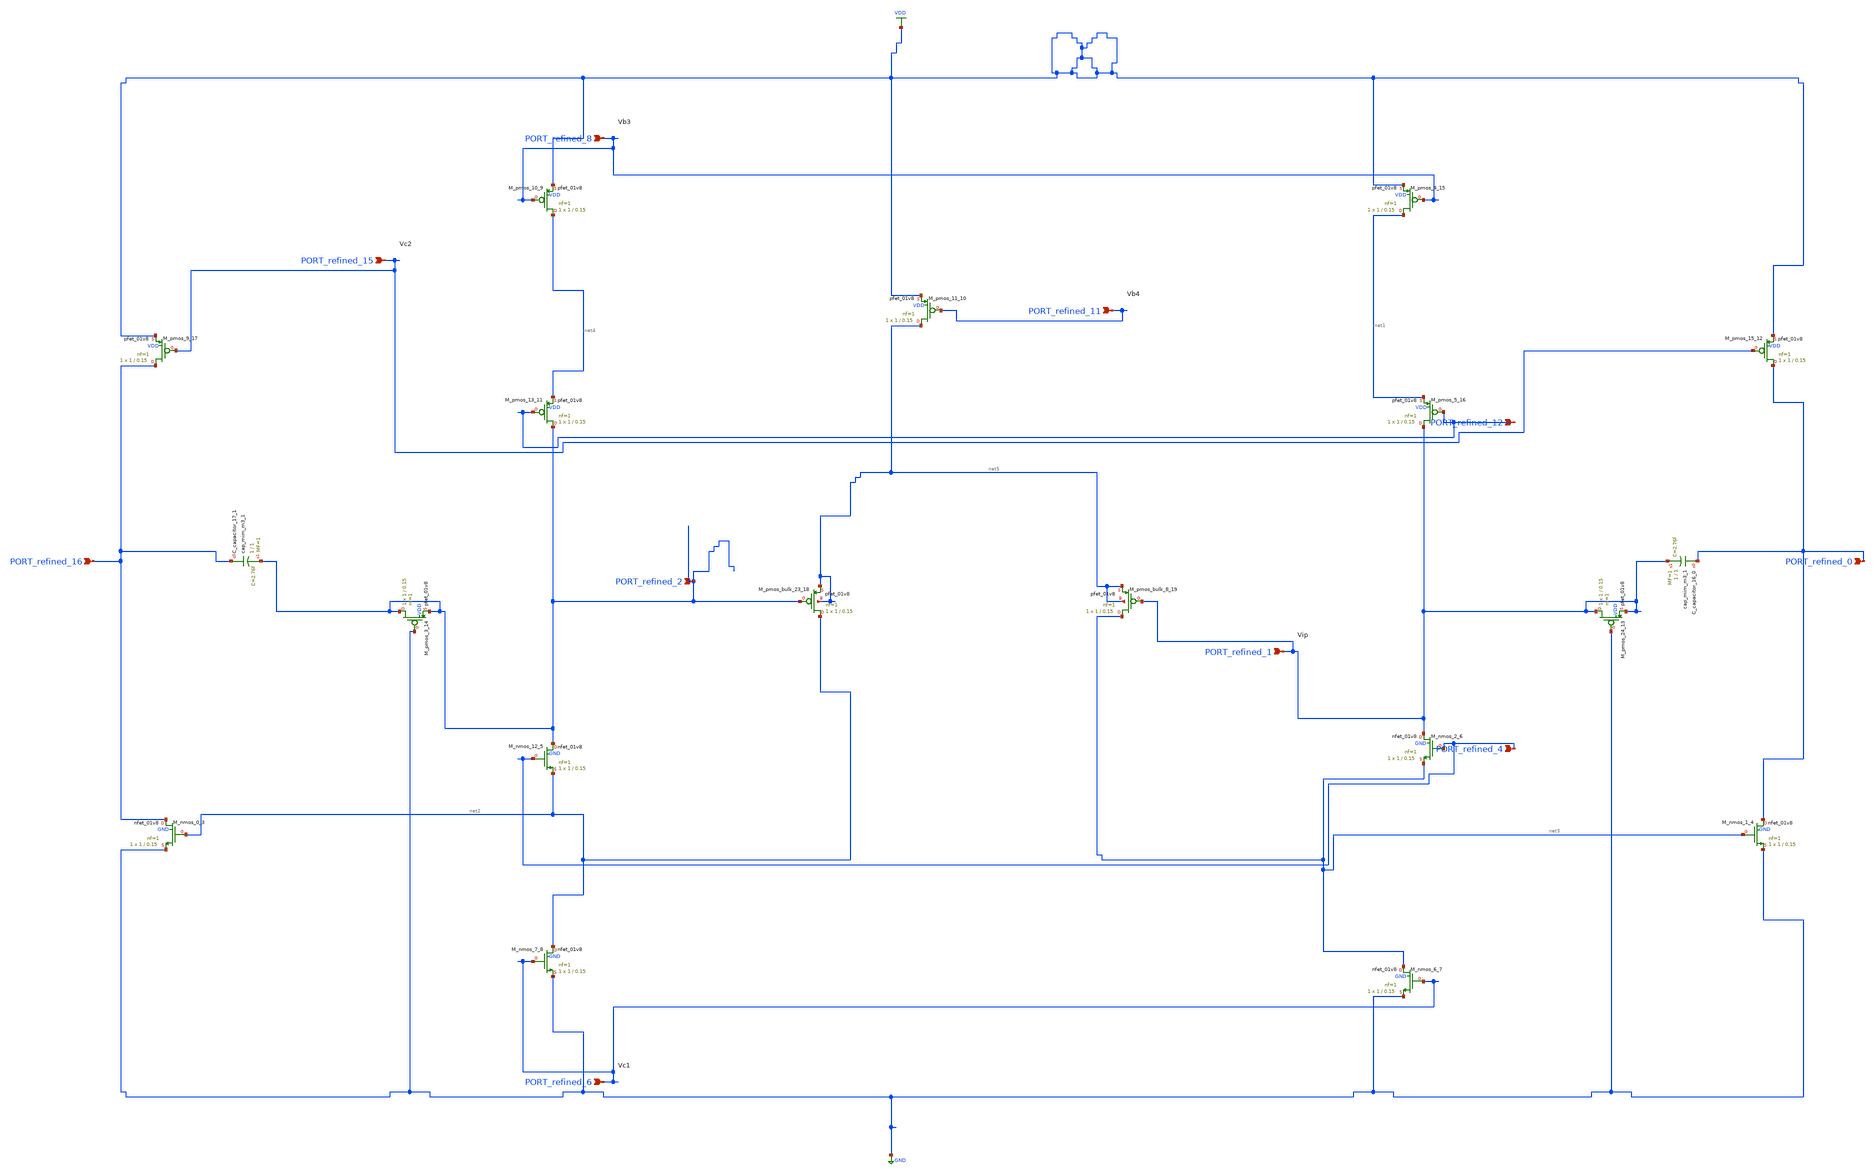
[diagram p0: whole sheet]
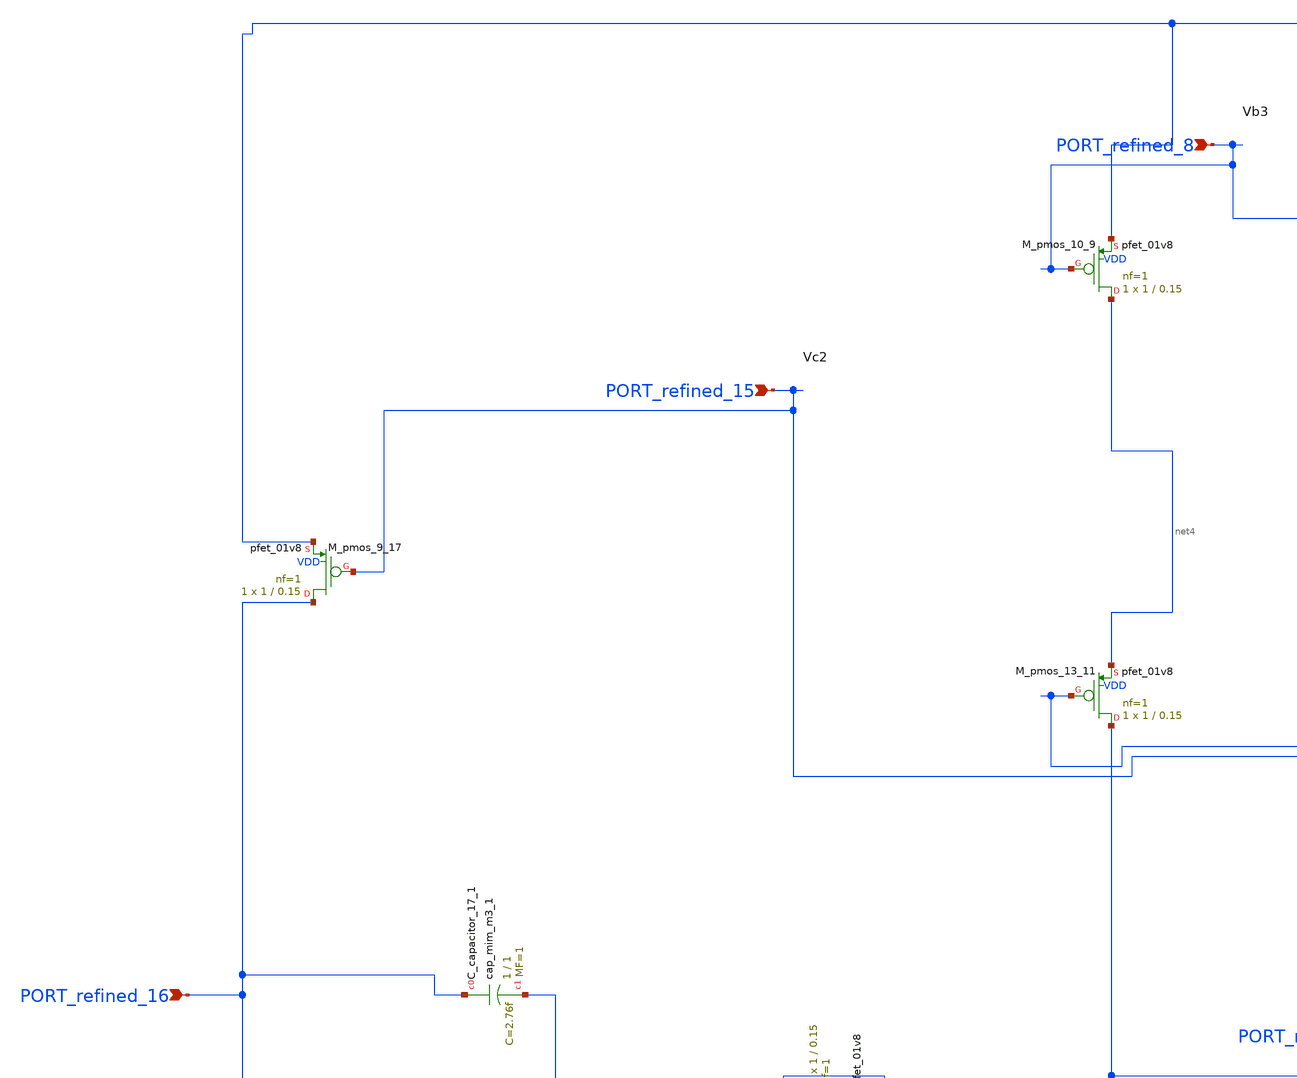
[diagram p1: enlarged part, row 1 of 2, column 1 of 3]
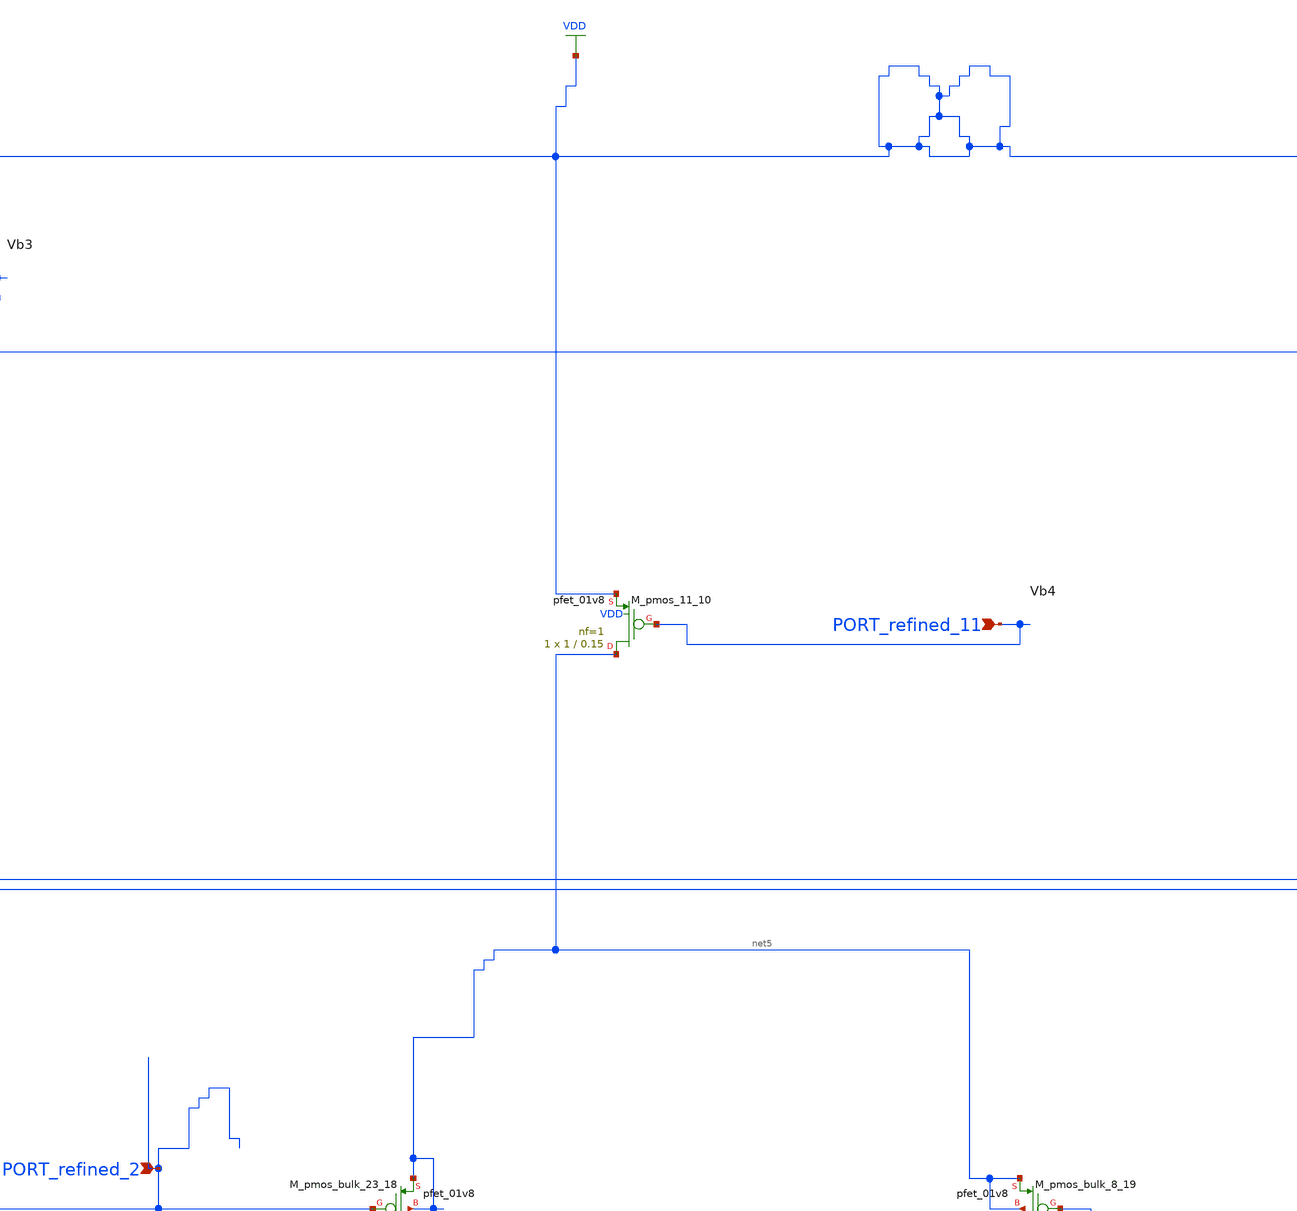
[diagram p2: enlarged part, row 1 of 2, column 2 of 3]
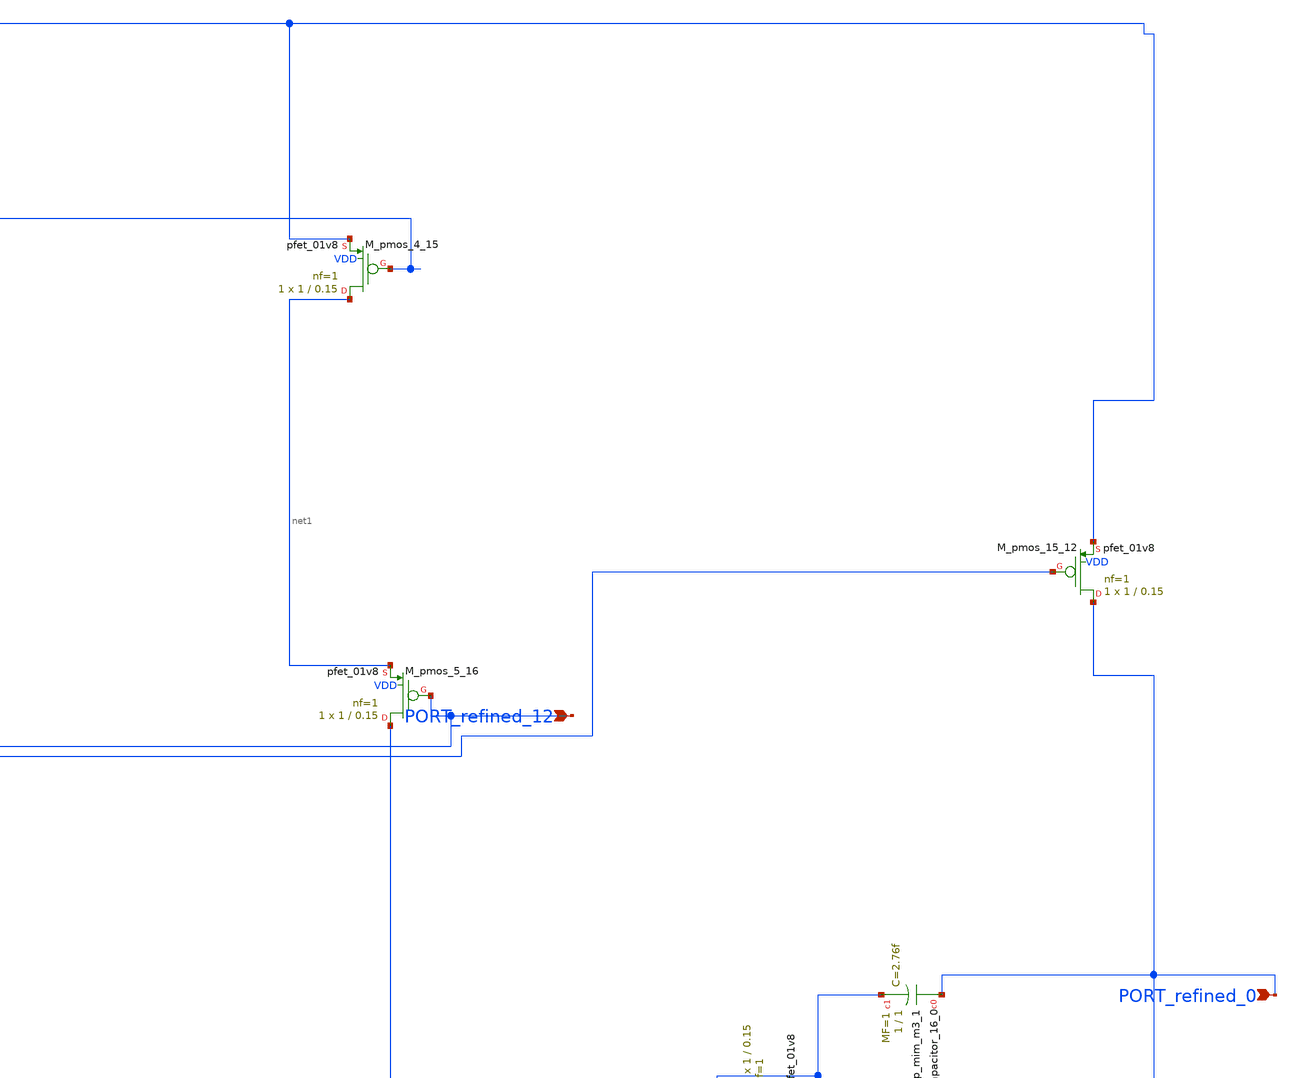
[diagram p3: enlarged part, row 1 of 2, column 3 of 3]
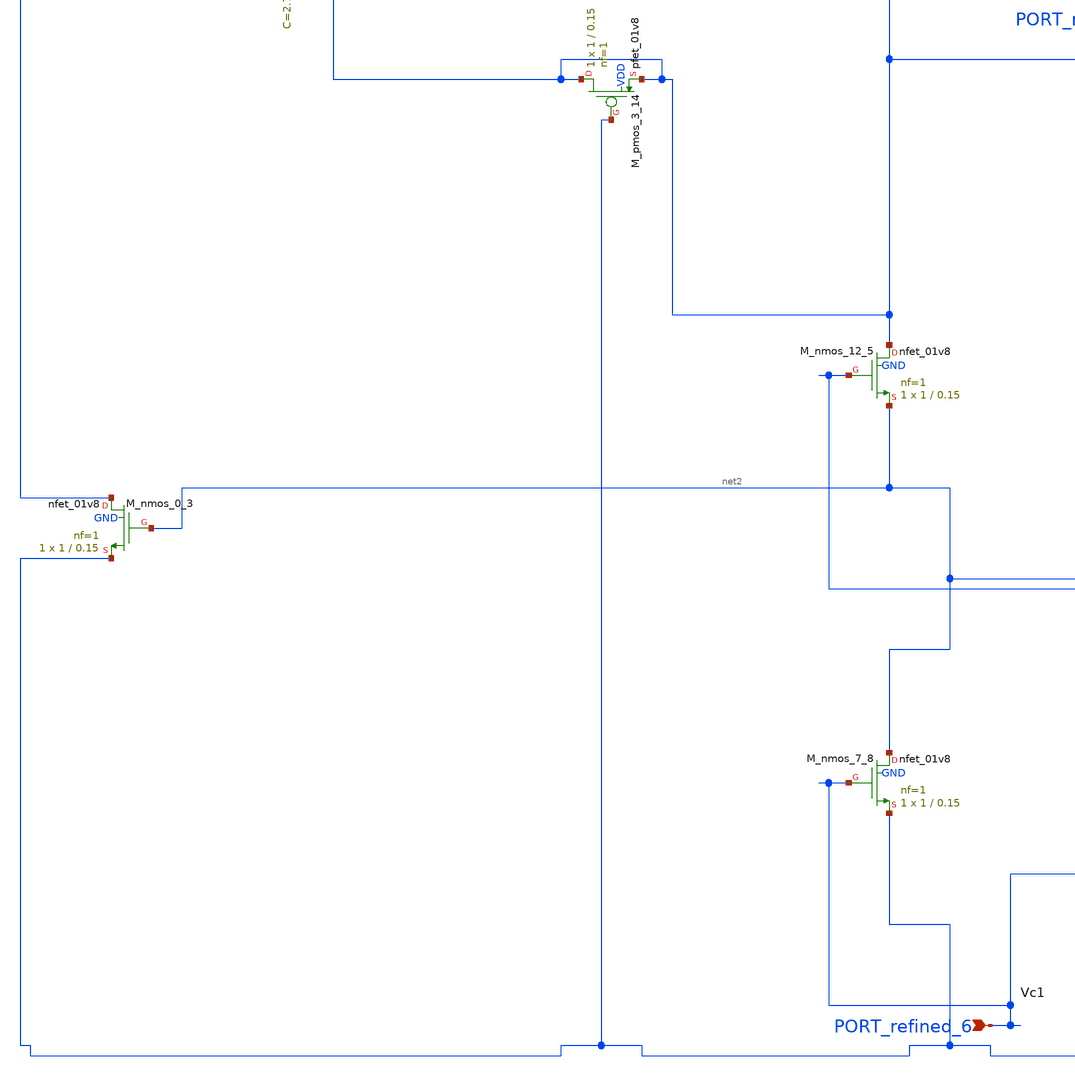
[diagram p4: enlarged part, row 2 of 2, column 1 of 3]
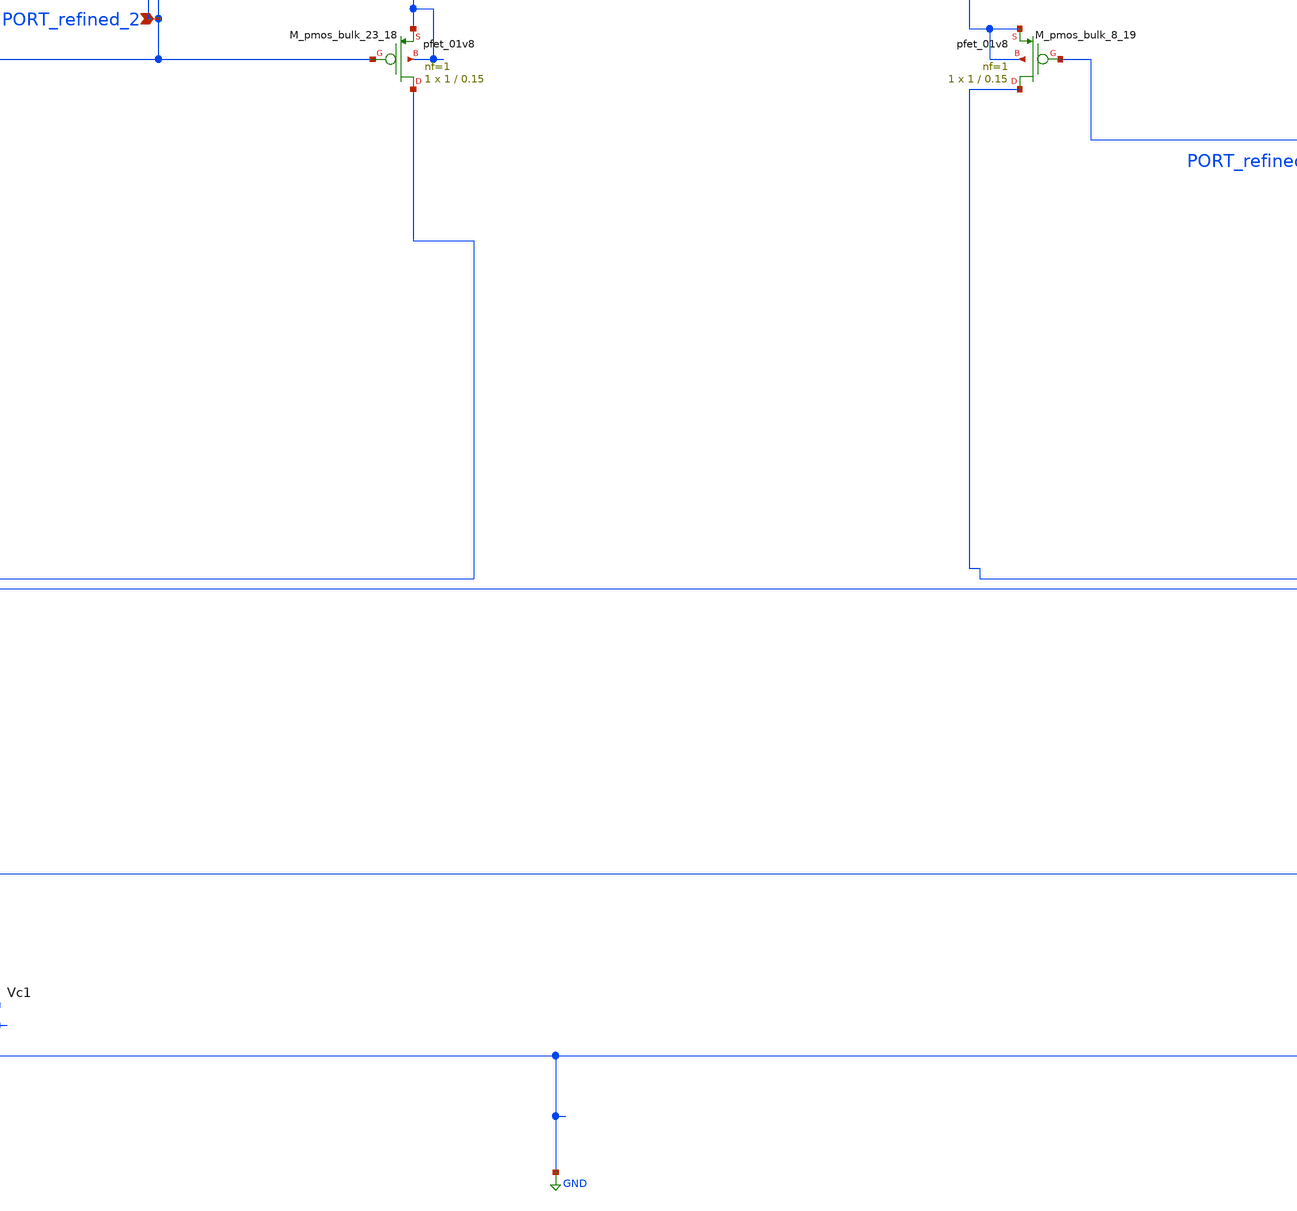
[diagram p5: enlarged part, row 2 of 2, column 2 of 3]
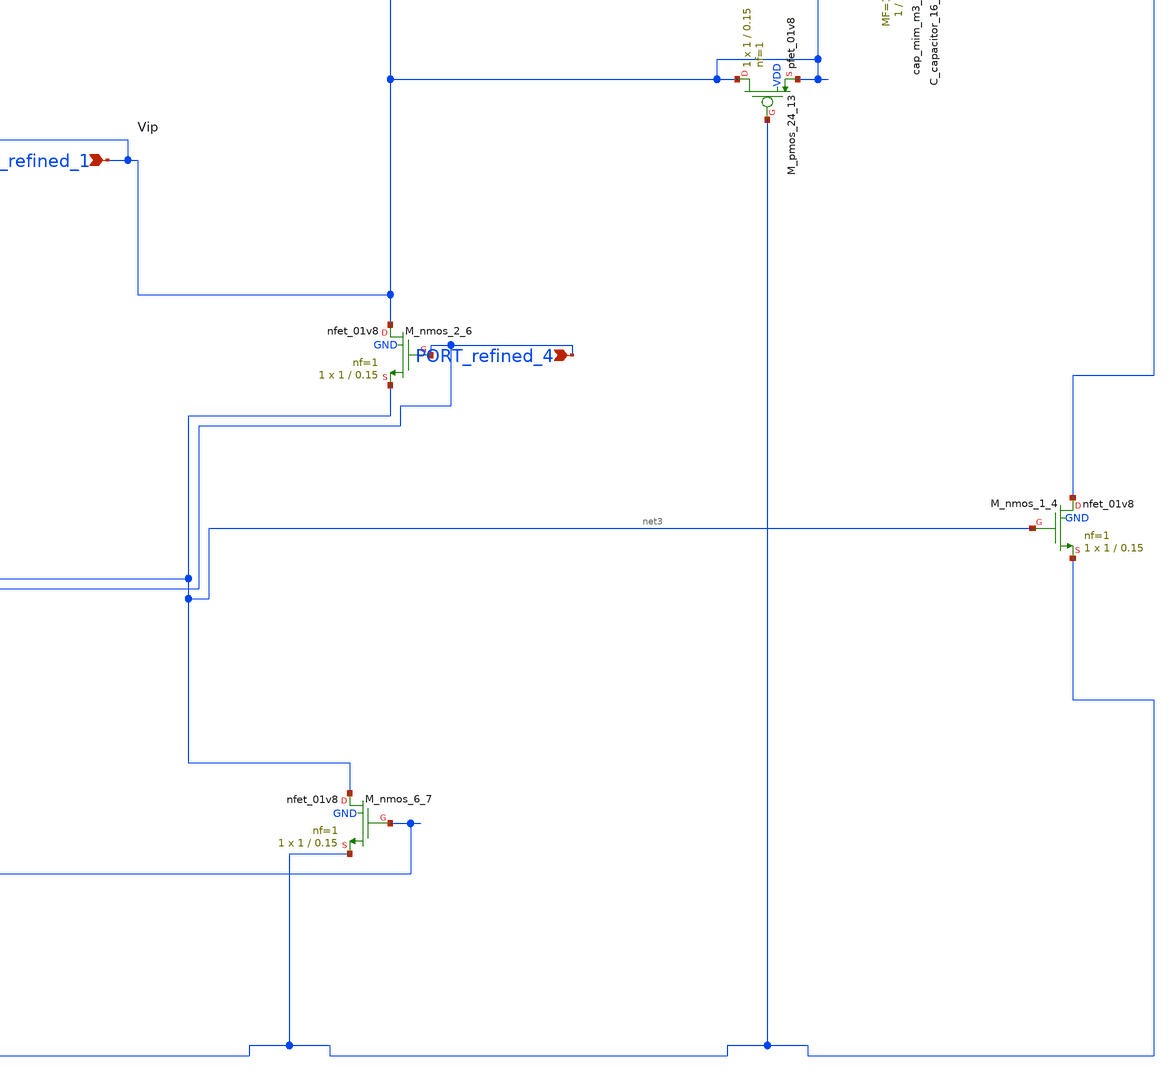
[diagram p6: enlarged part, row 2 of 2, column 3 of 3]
** sch_path: schematics/Image2Net/020.sch
**.subckt 020 PORT_refined_0 PORT_refined_16 PORT_refined_4 PORT_refined_12 PORT_refined_2
*+ PORT_refined_8 PORT_refined_6 PORT_refined_15 PORT_refined_11 PORT_refined_1
*.ipin PORT_refined_0
*.ipin PORT_refined_16
*.ipin PORT_refined_4
*.ipin PORT_refined_12
*.ipin PORT_refined_2
*.ipin PORT_refined_8
*.ipin PORT_refined_6
*.ipin PORT_refined_15
*.ipin PORT_refined_11
*.ipin PORT_refined_1
XC_capacitor_16_0 PORT_refined_0 PORT_refined_1 sky130_fd_pr__cap_mim_m3_1 W=1 L=1 MF=1 m=1
XC_capacitor_17_1 PORT_refined_16 PORT_refined_2 sky130_fd_pr__cap_mim_m3_1 W=1 L=1 MF=1 m=1
XM_nmos_0_3 PORT_refined_16 net2 GND GND sky130_fd_pr__nfet_01v8 L=0.15 W=1 nf=1 ad='int((1 + 1)/2) * 1 / 1 * 0.29'
+ as='int((1 + 2)/2) * 1 / 1 * 0.29' pd='2*int((1 + 1)/2) * (1 / 1 + 0.29)' ps='2*int((1 + 2)/2) * (1 / 1 + 0.29)'
+ nrd='0.29 / 1 ' nrs='0.29 / 1 ' sa=0 sb=0 sd=0 mult=1 m=1
XM_nmos_1_4 PORT_refined_0 net3 GND GND sky130_fd_pr__nfet_01v8 L=0.15 W=1 nf=1 ad='int((1 + 1)/2) * 1 / 1 * 0.29'
+ as='int((1 + 2)/2) * 1 / 1 * 0.29' pd='2*int((1 + 1)/2) * (1 / 1 + 0.29)' ps='2*int((1 + 2)/2) * (1 / 1 + 0.29)'
+ nrd='0.29 / 1 ' nrs='0.29 / 1 ' sa=0 sb=0 sd=0 mult=1 m=1
XM_nmos_12_5 PORT_refined_2 PORT_refined_4 net2 GND sky130_fd_pr__nfet_01v8 L=0.15 W=1 nf=1 ad='int((1 + 1)/2) * 1 / 1 * 0.29'
+ as='int((1 + 2)/2) * 1 / 1 * 0.29' pd='2*int((1 + 1)/2) * (1 / 1 + 0.29)' ps='2*int((1 + 2)/2) * (1 / 1 + 0.29)'
+ nrd='0.29 / 1 ' nrs='0.29 / 1 ' sa=0 sb=0 sd=0 mult=1 m=1
XM_nmos_2_6 PORT_refined_1 PORT_refined_4 net3 GND sky130_fd_pr__nfet_01v8 L=0.15 W=1 nf=1 ad='int((1 + 1)/2) * 1 / 1 * 0.29'
+ as='int((1 + 2)/2) * 1 / 1 * 0.29' pd='2*int((1 + 1)/2) * (1 / 1 + 0.29)' ps='2*int((1 + 2)/2) * (1 / 1 + 0.29)'
+ nrd='0.29 / 1 ' nrs='0.29 / 1 ' sa=0 sb=0 sd=0 mult=1 m=1
XM_nmos_6_7 net3 PORT_refined_6 GND GND sky130_fd_pr__nfet_01v8 L=0.15 W=1 nf=1 ad='int((1 + 1)/2) * 1 / 1 * 0.29'
+ as='int((1 + 2)/2) * 1 / 1 * 0.29' pd='2*int((1 + 1)/2) * (1 / 1 + 0.29)' ps='2*int((1 + 2)/2) * (1 / 1 + 0.29)'
+ nrd='0.29 / 1 ' nrs='0.29 / 1 ' sa=0 sb=0 sd=0 mult=1 m=1
XM_nmos_7_8 net2 PORT_refined_6 GND GND sky130_fd_pr__nfet_01v8 L=0.15 W=1 nf=1 ad='int((1 + 1)/2) * 1 / 1 * 0.29'
+ as='int((1 + 2)/2) * 1 / 1 * 0.29' pd='2*int((1 + 1)/2) * (1 / 1 + 0.29)' ps='2*int((1 + 2)/2) * (1 / 1 + 0.29)'
+ nrd='0.29 / 1 ' nrs='0.29 / 1 ' sa=0 sb=0 sd=0 mult=1 m=1
XM_pmos_10_9 net4 PORT_refined_8 VDD VDD sky130_fd_pr__pfet_01v8 L=0.15 W=1 nf=1 ad='int((1 + 1)/2) * 1 / 1 * 0.29'
+ as='int((1 + 2)/2) * 1 / 1 * 0.29' pd='2*int((1 + 1)/2) * (1 / 1 + 0.29)' ps='2*int((1 + 2)/2) * (1 / 1 + 0.29)'
+ nrd='0.29 / 1 ' nrs='0.29 / 1 ' sa=0 sb=0 sd=0 mult=1 m=1
XM_pmos_11_10 net5 PORT_refined_11 VDD VDD sky130_fd_pr__pfet_01v8 L=0.15 W=1 nf=1 ad='int((1 + 1)/2) * 1 / 1 * 0.29'
+ as='int((1 + 2)/2) * 1 / 1 * 0.29' pd='2*int((1 + 1)/2) * (1 / 1 + 0.29)' ps='2*int((1 + 2)/2) * (1 / 1 + 0.29)'
+ nrd='0.29 / 1 ' nrs='0.29 / 1 ' sa=0 sb=0 sd=0 mult=1 m=1
XM_pmos_13_11 PORT_refined_2 PORT_refined_12 net4 VDD sky130_fd_pr__pfet_01v8 L=0.15 W=1 nf=1 ad='int((1 + 1)/2) * 1 / 1 * 0.29'
+ as='int((1 + 2)/2) * 1 / 1 * 0.29' pd='2*int((1 + 1)/2) * (1 / 1 + 0.29)' ps='2*int((1 + 2)/2) * (1 / 1 + 0.29)'
+ nrd='0.29 / 1 ' nrs='0.29 / 1 ' sa=0 sb=0 sd=0 mult=1 m=1
XM_pmos_15_12 PORT_refined_0 PORT_refined_15 VDD VDD sky130_fd_pr__pfet_01v8 L=0.15 W=1 nf=1 ad='int((1 + 1)/2) * 1 / 1 * 0.29'
+ as='int((1 + 2)/2) * 1 / 1 * 0.29' pd='2*int((1 + 1)/2) * (1 / 1 + 0.29)' ps='2*int((1 + 2)/2) * (1 / 1 + 0.29)'
+ nrd='0.29 / 1 ' nrs='0.29 / 1 ' sa=0 sb=0 sd=0 mult=1 m=1
XM_pmos_24_13 PORT_refined_1 GND PORT_refined_1 VDD sky130_fd_pr__pfet_01v8 L=0.15 W=1 nf=1 ad='int((1 + 1)/2) * 1 / 1 * 0.29'
+ as='int((1 + 2)/2) * 1 / 1 * 0.29' pd='2*int((1 + 1)/2) * (1 / 1 + 0.29)' ps='2*int((1 + 2)/2) * (1 / 1 + 0.29)'
+ nrd='0.29 / 1 ' nrs='0.29 / 1 ' sa=0 sb=0 sd=0 mult=1 m=1
XM_pmos_3_14 PORT_refined_2 GND PORT_refined_2 VDD sky130_fd_pr__pfet_01v8 L=0.15 W=1 nf=1 ad='int((1 + 1)/2) * 1 / 1 * 0.29'
+ as='int((1 + 2)/2) * 1 / 1 * 0.29' pd='2*int((1 + 1)/2) * (1 / 1 + 0.29)' ps='2*int((1 + 2)/2) * (1 / 1 + 0.29)'
+ nrd='0.29 / 1 ' nrs='0.29 / 1 ' sa=0 sb=0 sd=0 mult=1 m=1
XM_pmos_4_15 net1 PORT_refined_8 VDD VDD sky130_fd_pr__pfet_01v8 L=0.15 W=1 nf=1 ad='int((1 + 1)/2) * 1 / 1 * 0.29'
+ as='int((1 + 2)/2) * 1 / 1 * 0.29' pd='2*int((1 + 1)/2) * (1 / 1 + 0.29)' ps='2*int((1 + 2)/2) * (1 / 1 + 0.29)'
+ nrd='0.29 / 1 ' nrs='0.29 / 1 ' sa=0 sb=0 sd=0 mult=1 m=1
XM_pmos_5_16 PORT_refined_1 PORT_refined_12 net1 VDD sky130_fd_pr__pfet_01v8 L=0.15 W=1 nf=1 ad='int((1 + 1)/2) * 1 / 1 * 0.29'
+ as='int((1 + 2)/2) * 1 / 1 * 0.29' pd='2*int((1 + 1)/2) * (1 / 1 + 0.29)' ps='2*int((1 + 2)/2) * (1 / 1 + 0.29)'
+ nrd='0.29 / 1 ' nrs='0.29 / 1 ' sa=0 sb=0 sd=0 mult=1 m=1
XM_pmos_9_17 PORT_refined_16 PORT_refined_15 VDD VDD sky130_fd_pr__pfet_01v8 L=0.15 W=1 nf=1 ad='int((1 + 1)/2) * 1 / 1 * 0.29'
+ as='int((1 + 2)/2) * 1 / 1 * 0.29' pd='2*int((1 + 1)/2) * (1 / 1 + 0.29)' ps='2*int((1 + 2)/2) * (1 / 1 + 0.29)'
+ nrd='0.29 / 1 ' nrs='0.29 / 1 ' sa=0 sb=0 sd=0 mult=1 m=1
XM_pmos_bulk_23_18 net2 PORT_refined_2 net5 net5 sky130_fd_pr__pfet_01v8 L=0.15 W=1 nf=1 ad='int((1 + 1)/2) * 1 / 1 * 0.29'
+ as='int((1 + 2)/2) * 1 / 1 * 0.29' pd='2*int((1 + 1)/2) * (1 / 1 + 0.29)' ps='2*int((1 + 2)/2) * (1 / 1 + 0.29)'
+ nrd='0.29 / 1 ' nrs='0.29 / 1 ' sa=0 sb=0 sd=0 mult=1 m=1
XM_pmos_bulk_8_19 net3 PORT_refined_1 net5 net5 sky130_fd_pr__pfet_01v8 L=0.15 W=1 nf=1 ad='int((1 + 1)/2) * 1 / 1 * 0.29'
+ as='int((1 + 2)/2) * 1 / 1 * 0.29' pd='2*int((1 + 1)/2) * (1 / 1 + 0.29)' ps='2*int((1 + 2)/2) * (1 / 1 + 0.29)'
+ nrd='0.29 / 1 ' nrs='0.29 / 1 ' sa=0 sb=0 sd=0 mult=1 m=1
**.ends
.GLOBAL GND
.GLOBAL VDD
.end
